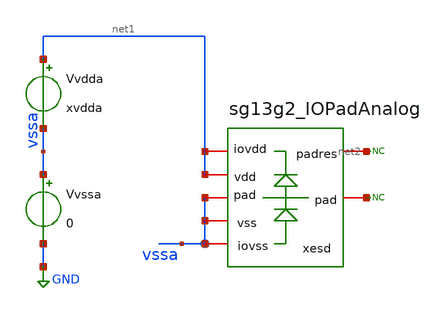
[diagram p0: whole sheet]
** sch_path: tb_OTA_1stage_ihp/esd_db.sch
**.subckt esd_db
* noconn #net2
xesd net1 vssa net2 net1 vssa vssa sg13g2_IOPadAnalog
Vvssa vssa GND 0
Vvdda net1 vssa xvdda
* noconn vssa
**.ends

* expanding   symbol:  sg13g2_IOPadAnalog.sym # of pins=7
** sym_path: tb_OTA_1stage_ihp/sg13g2_IOPadAnalog.sym
.include /home/slice/xschem/tb_OTA_1stage_ihp/PadRing/sg13g2_IOPadAnalog_RC.spice
.GLOBAL GND
.end
